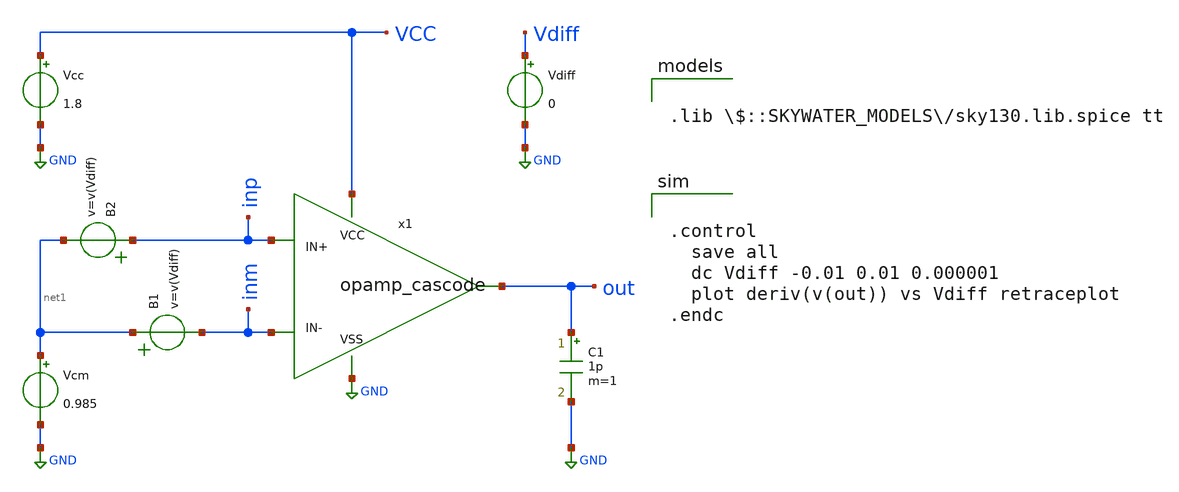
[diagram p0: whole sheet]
** sch_path: opamp_cascode_dc_max_gain.sch
**.subckt opamp_cascode_dc_max_gain
Vcc VCC GND 1.8
Vcm net1 GND 0.985
C1 out GND 1p m=1
x1 VCC GND inp inm out opamp_cascode
B1 net1 inm v=v(Vdiff)
Vdiff Vdiff GND 0
B2 inp net1 v=v(Vdiff)
**** begin user architecture code


.control
  save all
  dc Vdiff -0.01 0.01 0.000001
  plot deriv(v(out)) vs Vdiff retraceplot
.endc



.lib $::SKYWATER_MODELS/sky130.lib.spice tt

**** end user architecture code
**.ends

* expanding   symbol:  /home/zwierzak/projects/SKY130_OpAmp_GIT/opamp_cascode.sym # of pins=5
** sym_path: opamp_cascode.sym
** sch_path: opamp_cascode.sch
.subckt opamp_cascode VCC VSS IN+ IN- OUT
*.ipin IN+
*.ipin IN-
*.ipin VCC
*.ipin VSS
*.opin OUT
XM10 net8 net6 VCC VCC sky130_fd_pr__pfet_01v8 L=10 W=5 nf=1 ad='int((nf+1)/2) * W/nf * 0.29' as='int((nf+2)/2) * W/nf * 0.29'
+ pd='2*int((nf+1)/2) * (W/nf + 0.29)' ps='2*int((nf+2)/2) * (W/nf + 0.29)' nrd='0.29 / W' nrs='0.29 / W'
+ sa=0 sb=0 sd=0 mult=30 m=30
XM1 net7 net6 VCC VCC sky130_fd_pr__pfet_01v8 L=10 W=5 nf=1 ad='int((nf+1)/2) * W/nf * 0.29' as='int((nf+2)/2) * W/nf * 0.29'
+ pd='2*int((nf+1)/2) * (W/nf + 0.29)' ps='2*int((nf+2)/2) * (W/nf + 0.29)' nrd='0.29 / W' nrs='0.29 / W'
+ sa=0 sb=0 sd=0 mult=30 m=30
XM5 net3 net9 VCC VCC sky130_fd_pr__pfet_01v8 L=3 W=5 nf=1 ad='int((nf+1)/2) * W/nf * 0.29' as='int((nf+2)/2) * W/nf * 0.29'
+ pd='2*int((nf+1)/2) * (W/nf + 0.29)' ps='2*int((nf+2)/2) * (W/nf + 0.29)' nrd='0.29 / W' nrs='0.29 / W'
+ sa=0 sb=0 sd=0 mult=40 m=40
XM100 net9 net9 VCC VCC sky130_fd_pr__pfet_01v8 L=3 W=5 nf=1 ad='int((nf+1)/2) * W/nf * 0.29' as='int((nf+2)/2) * W/nf * 0.29'
+ pd='2*int((nf+1)/2) * (W/nf + 0.29)' ps='2*int((nf+2)/2) * (W/nf + 0.29)' nrd='0.29 / W' nrs='0.29 / W'
+ sa=0 sb=0 sd=0 mult=4 m=4
I0 net9 VSS 5.1u
XM11 OUT BIAS net8 net8 sky130_fd_pr__pfet_01v8 L=5 W=5 nf=1 ad='int((nf+1)/2) * W/nf * 0.29' as='int((nf+2)/2) * W/nf * 0.29'
+ pd='2*int((nf+1)/2) * (W/nf + 0.29)' ps='2*int((nf+2)/2) * (W/nf + 0.29)' nrd='0.29 / W' nrs='0.29 / W'
+ sa=0 sb=0 sd=0 mult=12 m=12
XM2 net6 BIAS net7 net7 sky130_fd_pr__pfet_01v8 L=5 W=5 nf=1 ad='int((nf+1)/2) * W/nf * 0.29' as='int((nf+2)/2) * W/nf * 0.29'
+ pd='2*int((nf+1)/2) * (W/nf + 0.29)' ps='2*int((nf+2)/2) * (W/nf + 0.29)' nrd='0.29 / W' nrs='0.29 / W'
+ sa=0 sb=0 sd=0 mult=12 m=12
XM6 net1 IN- net3 net3 sky130_fd_pr__pfet_01v8 L=0.18 W=5 nf=1 ad='int((nf+1)/2) * W/nf * 0.29' as='int((nf+2)/2) * W/nf * 0.29'
+ pd='2*int((nf+1)/2) * (W/nf + 0.29)' ps='2*int((nf+2)/2) * (W/nf + 0.29)' nrd='0.29 / W' nrs='0.29 / W'
+ sa=0 sb=0 sd=0 mult=50 m=50
XM8 net2 IN+ net3 net3 sky130_fd_pr__pfet_01v8 L=0.18 W=5 nf=1 ad='int((nf+1)/2) * W/nf * 0.29' as='int((nf+2)/2) * W/nf * 0.29'
+ pd='2*int((nf+1)/2) * (W/nf + 0.29)' ps='2*int((nf+2)/2) * (W/nf + 0.29)' nrd='0.29 / W' nrs='0.29 / W'
+ sa=0 sb=0 sd=0 mult=50 m=50
XM7 net1 net1 VSS VSS sky130_fd_pr__nfet_01v8 L=1 W=5 nf=1 ad='int((nf+1)/2) * W/nf * 0.29' as='int((nf+2)/2) * W/nf * 0.29'
+ pd='2*int((nf+1)/2) * (W/nf + 0.29)' ps='2*int((nf+2)/2) * (W/nf + 0.29)' nrd='0.29 / W' nrs='0.29 / W'
+ sa=0 sb=0 sd=0 mult=3 m=3
XM9 net2 net2 VSS VSS sky130_fd_pr__nfet_01v8 L=1 W=5 nf=1 ad='int((nf+1)/2) * W/nf * 0.29' as='int((nf+2)/2) * W/nf * 0.29'
+ pd='2*int((nf+1)/2) * (W/nf + 0.29)' ps='2*int((nf+2)/2) * (W/nf + 0.29)' nrd='0.29 / W' nrs='0.29 / W'
+ sa=0 sb=0 sd=0 mult=3 m=3
XM13 net4 net2 VSS VSS sky130_fd_pr__nfet_01v8 L=1 W=5 nf=1 ad='int((nf+1)/2) * W/nf * 0.29' as='int((nf+2)/2) * W/nf * 0.29'
+ pd='2*int((nf+1)/2) * (W/nf + 0.29)' ps='2*int((nf+2)/2) * (W/nf + 0.29)' nrd='0.29 / W' nrs='0.29 / W'
+ sa=0 sb=0 sd=0 mult=6 m=6
XM4 net5 net1 VSS VSS sky130_fd_pr__nfet_01v8 L=1 W=5 nf=1 ad='int((nf+1)/2) * W/nf * 0.29' as='int((nf+2)/2) * W/nf * 0.29'
+ pd='2*int((nf+1)/2) * (W/nf + 0.29)' ps='2*int((nf+2)/2) * (W/nf + 0.29)' nrd='0.29 / W' nrs='0.29 / W'
+ sa=0 sb=0 sd=0 mult=6 m=6
XM12 OUT BIAS1 net4 net4 sky130_fd_pr__nfet_01v8 L=3 W=5 nf=1 ad='int((nf+1)/2) * W/nf * 0.29' as='int((nf+2)/2) * W/nf * 0.29'
+ pd='2*int((nf+1)/2) * (W/nf + 0.29)' ps='2*int((nf+2)/2) * (W/nf + 0.29)' nrd='0.29 / W' nrs='0.29 / W'
+ sa=0 sb=0 sd=0 mult=9 m=9
XM3 net6 BIAS1 net5 net5 sky130_fd_pr__nfet_01v8 L=3 W=5 nf=1 ad='int((nf+1)/2) * W/nf * 0.29' as='int((nf+2)/2) * W/nf * 0.29'
+ pd='2*int((nf+1)/2) * (W/nf + 0.29)' ps='2*int((nf+2)/2) * (W/nf + 0.29)' nrd='0.29 / W' nrs='0.29 / W'
+ sa=0 sb=0 sd=0 mult=9 m=9
V1 BIAS VSS 0.12
V2 BIAS1 VSS 0.7
.ends

.GLOBAL GND
.end
